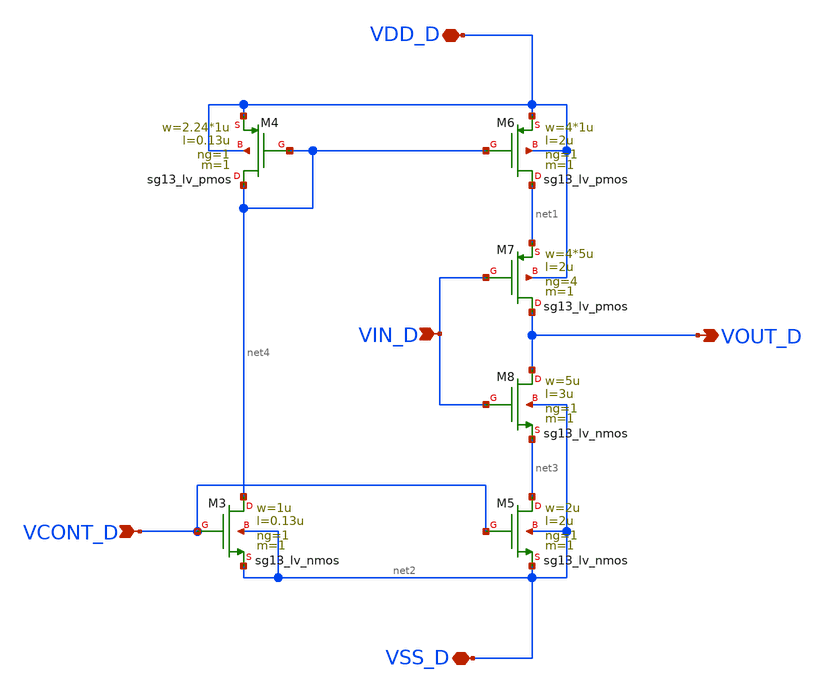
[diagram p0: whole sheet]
** sch_path: sch/delay_variable/delay_variable.sch
**.subckt delay_variable VSS_D VDD_D VOUT_D VCONT_D VIN_D
*.iopin VSS_D
*.iopin VDD_D
*.opin VOUT_D
*.ipin VCONT_D
*.ipin VIN_D
XM3 net4 VCONT_D net2 net2 sg13_lv_nmos w=1u l=0.13u ng=1 m=1 mm_ok=1
XM5 net3 VCONT_D net2 net2 sg13_lv_nmos w=2u l=2u ng=1 m=1 mm_ok=1
XM4 net4 net4 VDD_D VDD_D sg13_lv_pmos w=2.24*1u l=0.13u ng=1 m=1 mm_ok=1
XM6 net1 net4 VDD_D VDD_D sg13_lv_pmos w=4*1u l=2u ng=1 m=1 mm_ok=1
XM7 VOUT_D VIN_D net1 VDD_D sg13_lv_pmos w=4*5u l=2u ng=4 m=1 mm_ok=1
XM8 VOUT_D VIN_D net3 net2 sg13_lv_nmos w=5u l=3u ng=1 m=1 mm_ok=1
**.ends
.end
